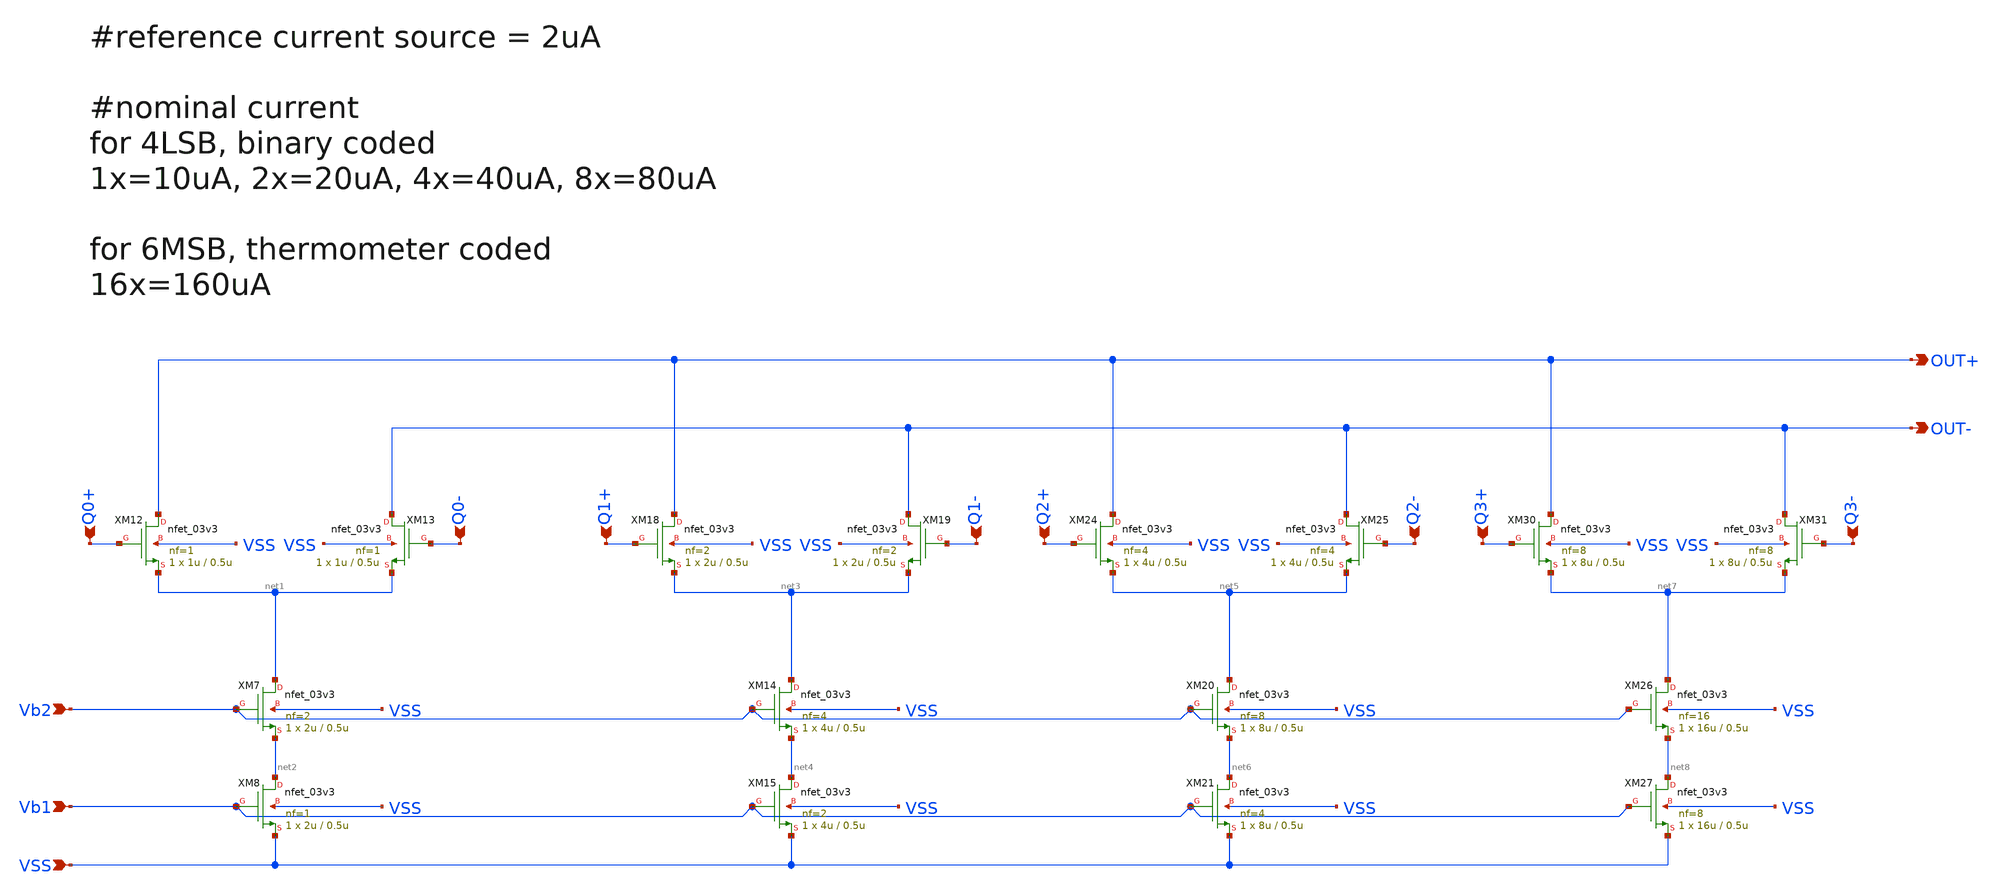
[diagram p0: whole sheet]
** sch_path: DAC/xschem/dac_lsb_analog.sch
**.subckt dac_lsb_analog VSS Vb2 Vb1 Q3- Q3+ Q2- Q2+ Q1- Q1+ Q0- Q0+ OUT+ OUT-
*.ipin VSS
*.ipin Vb2
*.ipin Vb1
*.ipin Q3-
*.ipin Q3+
*.ipin Q2-
*.ipin Q2+
*.ipin Q1-
*.ipin Q1+
*.ipin Q0-
*.ipin Q0+
*.opin OUT+
*.opin OUT-
XM7 net1 Vb2 net2 VSS nfet_03v3 L=0.5u W=2u nf=2 ad='int((nf+1)/2) * W/nf * 0.18u' as='int((nf+2)/2) * W/nf * 0.18u'
+ pd='2*int((nf+1)/2) * (W/nf + 0.18u)' ps='2*int((nf+2)/2) * (W/nf + 0.18u)' nrd='0.18u / W' nrs='0.18u / W'
+ sa=0 sb=0 sd=0 m=1
XM8 net2 Vb1 VSS VSS nfet_03v3 L=0.5u W=2u nf=1 ad='int((nf+1)/2) * W/nf * 0.18u' as='int((nf+2)/2) * W/nf * 0.18u'
+ pd='2*int((nf+1)/2) * (W/nf + 0.18u)' ps='2*int((nf+2)/2) * (W/nf + 0.18u)' nrd='0.18u / W' nrs='0.18u / W'
+ sa=0 sb=0 sd=0 m=1
XM12 OUT+ Q0+ net1 VSS nfet_03v3 L=0.5u W=1u nf=1 ad='int((nf+1)/2) * W/nf * 0.18u' as='int((nf+2)/2) * W/nf * 0.18u'
+ pd='2*int((nf+1)/2) * (W/nf + 0.18u)' ps='2*int((nf+2)/2) * (W/nf + 0.18u)' nrd='0.18u / W' nrs='0.18u / W'
+ sa=0 sb=0 sd=0 m=1
XM13 OUT- Q0- net1 VSS nfet_03v3 L=0.5u W=1u nf=1 ad='int((nf+1)/2) * W/nf * 0.18u' as='int((nf+2)/2) * W/nf * 0.18u'
+ pd='2*int((nf+1)/2) * (W/nf + 0.18u)' ps='2*int((nf+2)/2) * (W/nf + 0.18u)' nrd='0.18u / W' nrs='0.18u / W'
+ sa=0 sb=0 sd=0 m=1
XM14 net3 Vb2 net4 VSS nfet_03v3 L=0.5u W=4u nf=4 ad='int((nf+1)/2) * W/nf * 0.18u' as='int((nf+2)/2) * W/nf * 0.18u'
+ pd='2*int((nf+1)/2) * (W/nf + 0.18u)' ps='2*int((nf+2)/2) * (W/nf + 0.18u)' nrd='0.18u / W' nrs='0.18u / W'
+ sa=0 sb=0 sd=0 m=1
XM15 net4 Vb1 VSS VSS nfet_03v3 L=0.5u W=4u nf=2 ad='int((nf+1)/2) * W/nf * 0.18u' as='int((nf+2)/2) * W/nf * 0.18u'
+ pd='2*int((nf+1)/2) * (W/nf + 0.18u)' ps='2*int((nf+2)/2) * (W/nf + 0.18u)' nrd='0.18u / W' nrs='0.18u / W'
+ sa=0 sb=0 sd=0 m=1
XM18 OUT+ Q1+ net3 VSS nfet_03v3 L=0.5u W=2u nf=2 ad='int((nf+1)/2) * W/nf * 0.18u' as='int((nf+2)/2) * W/nf * 0.18u'
+ pd='2*int((nf+1)/2) * (W/nf + 0.18u)' ps='2*int((nf+2)/2) * (W/nf + 0.18u)' nrd='0.18u / W' nrs='0.18u / W'
+ sa=0 sb=0 sd=0 m=1
XM19 OUT- Q1- net3 VSS nfet_03v3 L=0.5u W=2u nf=2 ad='int((nf+1)/2) * W/nf * 0.18u' as='int((nf+2)/2) * W/nf * 0.18u'
+ pd='2*int((nf+1)/2) * (W/nf + 0.18u)' ps='2*int((nf+2)/2) * (W/nf + 0.18u)' nrd='0.18u / W' nrs='0.18u / W'
+ sa=0 sb=0 sd=0 m=1
XM20 net5 Vb2 net6 VSS nfet_03v3 L=0.5u W=8u nf=8 ad='int((nf+1)/2) * W/nf * 0.18u' as='int((nf+2)/2) * W/nf * 0.18u'
+ pd='2*int((nf+1)/2) * (W/nf + 0.18u)' ps='2*int((nf+2)/2) * (W/nf + 0.18u)' nrd='0.18u / W' nrs='0.18u / W'
+ sa=0 sb=0 sd=0 m=1
XM21 net6 Vb1 VSS VSS nfet_03v3 L=0.5u W=8u nf=4 ad='int((nf+1)/2) * W/nf * 0.18u' as='int((nf+2)/2) * W/nf * 0.18u'
+ pd='2*int((nf+1)/2) * (W/nf + 0.18u)' ps='2*int((nf+2)/2) * (W/nf + 0.18u)' nrd='0.18u / W' nrs='0.18u / W'
+ sa=0 sb=0 sd=0 m=1
XM24 OUT+ Q2+ net5 VSS nfet_03v3 L=0.5u W=4u nf=4 ad='int((nf+1)/2) * W/nf * 0.18u' as='int((nf+2)/2) * W/nf * 0.18u'
+ pd='2*int((nf+1)/2) * (W/nf + 0.18u)' ps='2*int((nf+2)/2) * (W/nf + 0.18u)' nrd='0.18u / W' nrs='0.18u / W'
+ sa=0 sb=0 sd=0 m=1
XM25 OUT- Q2- net5 VSS nfet_03v3 L=0.5u W=4u nf=4 ad='int((nf+1)/2) * W/nf * 0.18u' as='int((nf+2)/2) * W/nf * 0.18u'
+ pd='2*int((nf+1)/2) * (W/nf + 0.18u)' ps='2*int((nf+2)/2) * (W/nf + 0.18u)' nrd='0.18u / W' nrs='0.18u / W'
+ sa=0 sb=0 sd=0 m=1
XM26 net7 Vb2 net8 VSS nfet_03v3 L=0.5u W=16u nf=16 ad='int((nf+1)/2) * W/nf * 0.18u' as='int((nf+2)/2) * W/nf * 0.18u'
+ pd='2*int((nf+1)/2) * (W/nf + 0.18u)' ps='2*int((nf+2)/2) * (W/nf + 0.18u)' nrd='0.18u / W' nrs='0.18u / W'
+ sa=0 sb=0 sd=0 m=1
XM27 net8 Vb1 VSS VSS nfet_03v3 L=0.5u W=16u nf=8 ad='int((nf+1)/2) * W/nf * 0.18u' as='int((nf+2)/2) * W/nf * 0.18u'
+ pd='2*int((nf+1)/2) * (W/nf + 0.18u)' ps='2*int((nf+2)/2) * (W/nf + 0.18u)' nrd='0.18u / W' nrs='0.18u / W'
+ sa=0 sb=0 sd=0 m=1
XM30 OUT+ Q3+ net7 VSS nfet_03v3 L=0.5u W=8u nf=8 ad='int((nf+1)/2) * W/nf * 0.18u' as='int((nf+2)/2) * W/nf * 0.18u'
+ pd='2*int((nf+1)/2) * (W/nf + 0.18u)' ps='2*int((nf+2)/2) * (W/nf + 0.18u)' nrd='0.18u / W' nrs='0.18u / W'
+ sa=0 sb=0 sd=0 m=1
XM31 OUT- Q3- net7 VSS nfet_03v3 L=0.5u W=8u nf=8 ad='int((nf+1)/2) * W/nf * 0.18u' as='int((nf+2)/2) * W/nf * 0.18u'
+ pd='2*int((nf+1)/2) * (W/nf + 0.18u)' ps='2*int((nf+2)/2) * (W/nf + 0.18u)' nrd='0.18u / W' nrs='0.18u / W'
+ sa=0 sb=0 sd=0 m=1
**.ends
.end
